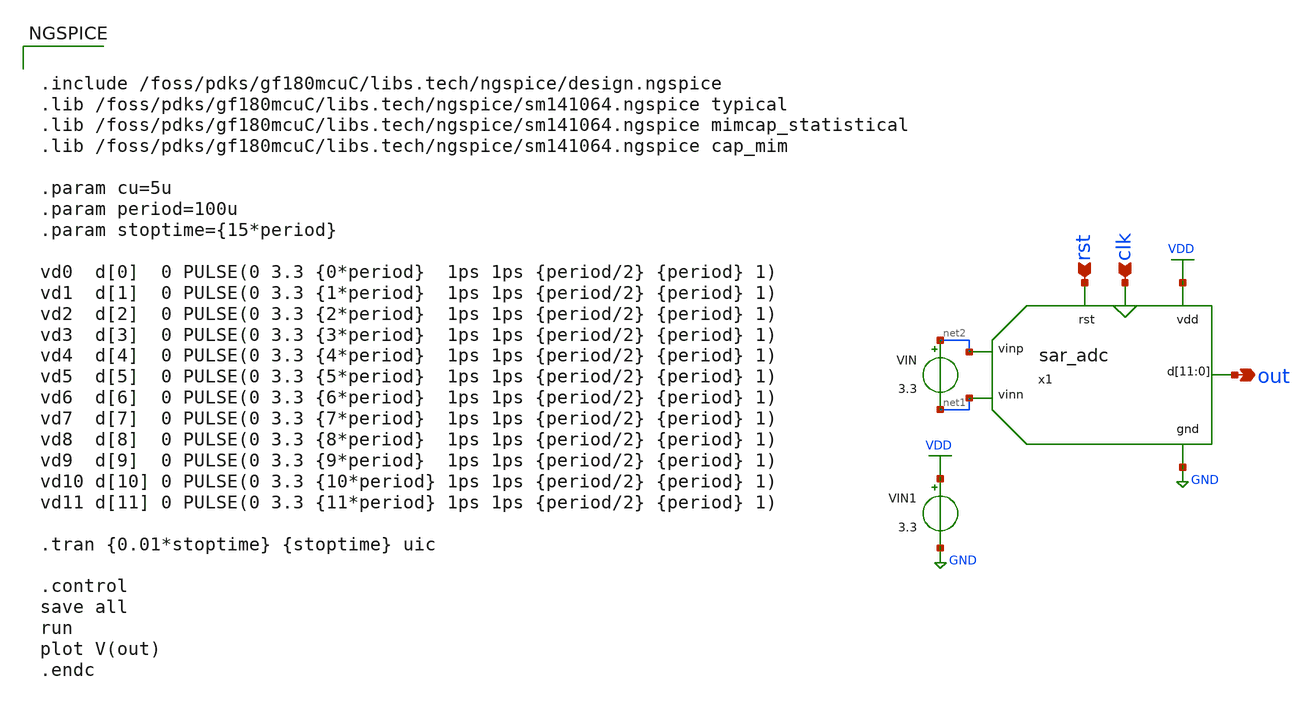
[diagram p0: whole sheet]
** sch_path: SAR_ADC/xschem/test/tb_sar_adc.sch
**.subckt tb_sar_adc rst clk out
*.ipin rst
*.ipin clk
*.opin out
x1 net2 out out out out out out out out out out out out rst clk net1 GND VDD sar_adc
VIN net2 net1 3.3
VIN1 VDD GND 3.3
**** begin user architecture code


.include /foss/pdks/gf180mcuC/libs.tech/ngspice/design.ngspice
.lib /foss/pdks/gf180mcuC/libs.tech/ngspice/sm141064.ngspice typical
.lib /foss/pdks/gf180mcuC/libs.tech/ngspice/sm141064.ngspice mimcap_statistical
.lib /foss/pdks/gf180mcuC/libs.tech/ngspice/sm141064.ngspice cap_mim

.param cu=5u
.param period=100u
.param stoptime={15*period}

vd0  d[0]  0 PULSE(0 3.3 {0*period}  1ps 1ps {period/2} {period} 1)
vd1  d[1]  0 PULSE(0 3.3 {1*period}  1ps 1ps {period/2} {period} 1)
vd2  d[2]  0 PULSE(0 3.3 {2*period}  1ps 1ps {period/2} {period} 1)
vd3  d[3]  0 PULSE(0 3.3 {3*period}  1ps 1ps {period/2} {period} 1)
vd4  d[4]  0 PULSE(0 3.3 {4*period}  1ps 1ps {period/2} {period} 1)
vd5  d[5]  0 PULSE(0 3.3 {5*period}  1ps 1ps {period/2} {period} 1)
vd6  d[6]  0 PULSE(0 3.3 {6*period}  1ps 1ps {period/2} {period} 1)
vd7  d[7]  0 PULSE(0 3.3 {7*period}  1ps 1ps {period/2} {period} 1)
vd8  d[8]  0 PULSE(0 3.3 {8*period}  1ps 1ps {period/2} {period} 1)
vd9  d[9]  0 PULSE(0 3.3 {9*period}  1ps 1ps {period/2} {period} 1)
vd10 d[10] 0 PULSE(0 3.3 {10*period} 1ps 1ps {period/2} {period} 1)
vd11 d[11] 0 PULSE(0 3.3 {11*period} 1ps 1ps {period/2} {period} 1)

.tran {0.01*stoptime} {stoptime} uic

.control
save all
run
plot V(out)
.endc


**** end user architecture code
**.ends
.GLOBAL VDD
.GLOBAL GND
.end
